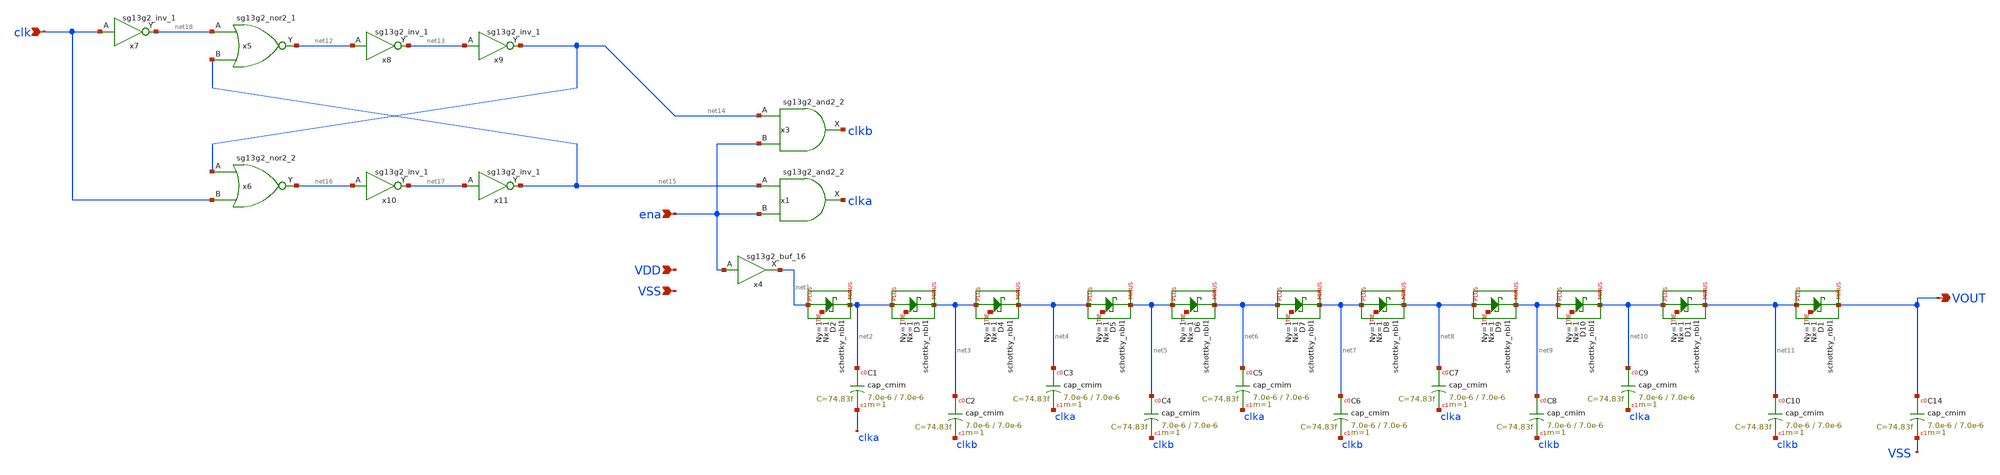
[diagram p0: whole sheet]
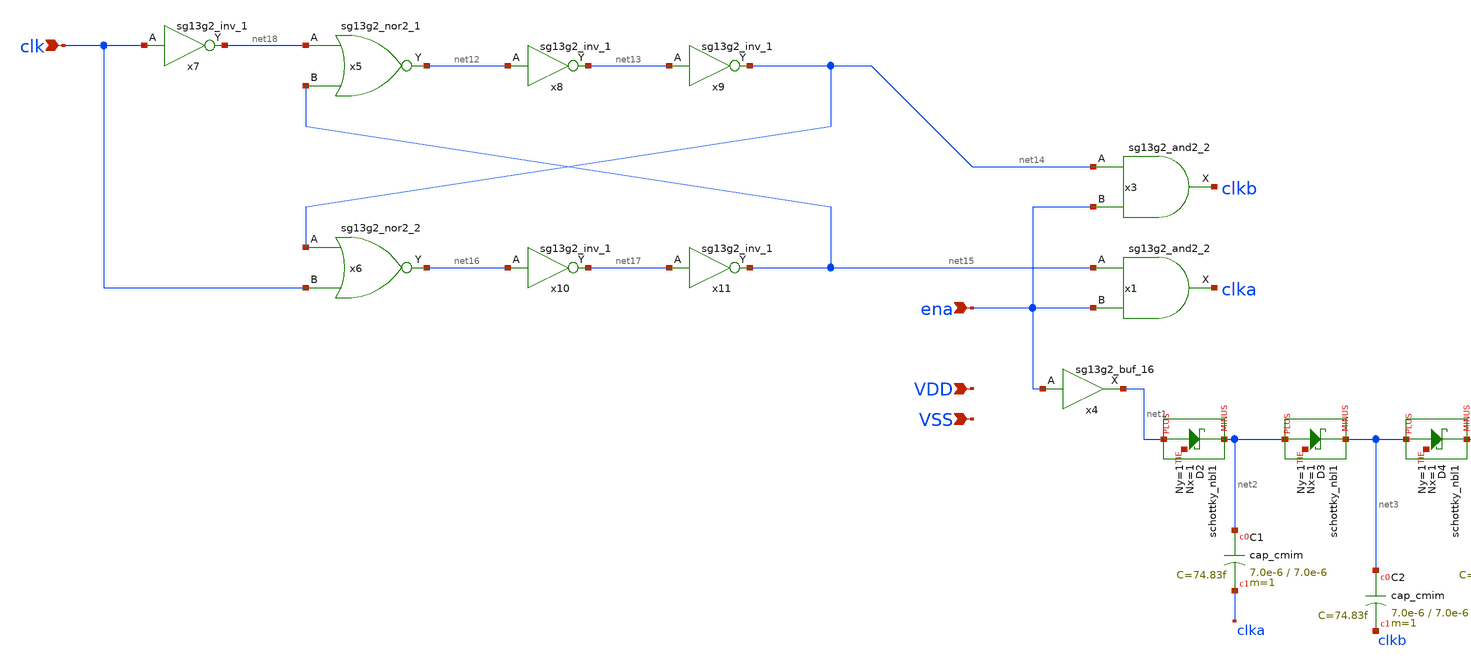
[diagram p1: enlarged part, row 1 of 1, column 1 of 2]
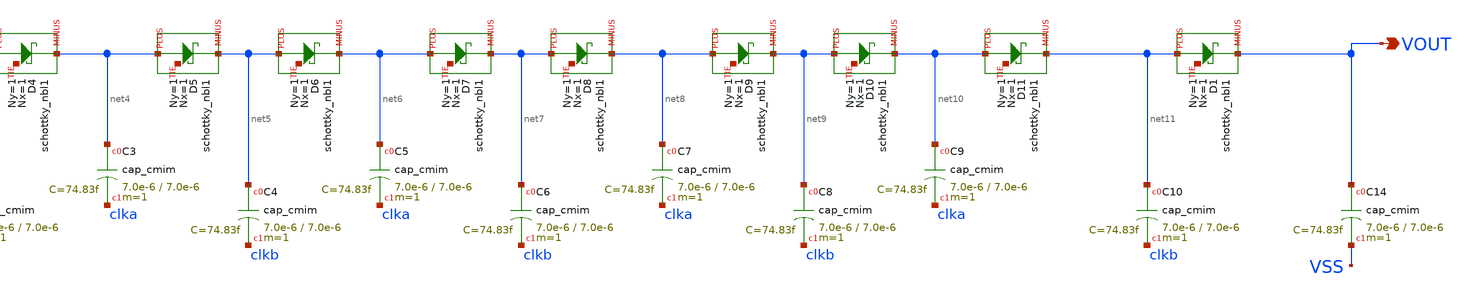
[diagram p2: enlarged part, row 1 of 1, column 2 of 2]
** sch_path: ihp130_cells/Schottky_PosChargePump/schottky_pump.sch
* IHP-GmbH/IHP-Open-PDK/ihp-sg13g2/libs.tech/xschem/sg13g2_stdcells/sg13g2_nor2_1.sch:
* Copyright 2023 IHP PDK Authors
* Licensed under the Apache License, Version 2.0 (the "License");
**.subckt schottky_pump clk ena VDD VSS VOUT
*.ipin clk
*.ipin ena
*.ipin VDD
*.ipin VSS
*.opin VOUT
XC1 net2 clka cap_cmim w=7.0e-6 l=7.0e-6 m=1 mm_ok=1
x1 clka net15 ena VDD VSS sg13g2_and2_2
x3 clkb net14 ena VDD VSS sg13g2_and2_2
x4 net1 ena VDD VSS sg13g2_buf_16
XD2 net1 net2 net19 schottky_nbl1 Nx=1 Ny=1
XD3 net2 net3 net20 schottky_nbl1 Nx=1 Ny=1
XD4 net3 net4 net21 schottky_nbl1 Nx=1 Ny=1
XD5 net4 net5 net22 schottky_nbl1 Nx=1 Ny=1
XD6 net5 net6 net23 schottky_nbl1 Nx=1 Ny=1
XD7 net6 net7 net24 schottky_nbl1 Nx=1 Ny=1
XD8 net7 net8 net25 schottky_nbl1 Nx=1 Ny=1
XD9 net8 net9 net26 schottky_nbl1 Nx=1 Ny=1
XD10 net9 net10 net27 schottky_nbl1 Nx=1 Ny=1
XD11 net10 net11 net28 schottky_nbl1 Nx=1 Ny=1
XC2 net3 clkb cap_cmim w=7.0e-6 l=7.0e-6 m=1 mm_ok=1
XC3 net4 clka cap_cmim w=7.0e-6 l=7.0e-6 m=1 mm_ok=1
XC4 net5 clkb cap_cmim w=7.0e-6 l=7.0e-6 m=1 mm_ok=1
XC5 net6 clka cap_cmim w=7.0e-6 l=7.0e-6 m=1 mm_ok=1
XC6 net7 clkb cap_cmim w=7.0e-6 l=7.0e-6 m=1 mm_ok=1
XC7 net8 clka cap_cmim w=7.0e-6 l=7.0e-6 m=1 mm_ok=1
XC8 net9 clkb cap_cmim w=7.0e-6 l=7.0e-6 m=1 mm_ok=1
XC9 net10 clka cap_cmim w=7.0e-6 l=7.0e-6 m=1 mm_ok=1
XC14 VOUT VSS cap_cmim w=7.0e-6 l=7.0e-6 m=1 mm_ok=1
XD1 net11 VOUT net29 schottky_nbl1 Nx=1 Ny=1
XC10 net11 clkb cap_cmim w=7.0e-6 l=7.0e-6 m=1 mm_ok=1
x5 net12 net18 net15 VDD VSS sg13g2_nor2_1
x6 net16 net14 clk VDD VSS sg13g2_nor2_2
x7 net18 clk VDD VSS sg13g2_inv_1
x8 net13 net12 VDD VSS sg13g2_inv_1
x9 net14 net13 VDD VSS sg13g2_inv_1
x10 net17 net16 VDD VSS sg13g2_inv_1
x11 net15 net17 VDD VSS sg13g2_inv_1
**.ends

* expanding   symbol:  sg13g2_stdcells/sg13g2_and2_2.sym # of pins=3
** sym_path: sg13g2_stdcells/sg13g2_and2_2.sym
** sch_path: sg13g2_stdcells/sg13g2_and2_2.sch
.subckt sg13g2_and2_2 X A B VDD VSS
*.ipin A
*.ipin B
*.opin X
*.iopin VDD
*.iopin VSS
XM1 net1 A net2 VSS sg13_lv_nmos w=640.00n l=130.00n ng=1 m=1 mm_ok=1
XM2 net2 B VSS VSS sg13_lv_nmos w=640.00n l=130.00n ng=1 m=1 mm_ok=1
XM3 X net1 VSS VSS sg13_lv_nmos w=1.48u l=130.00n ng=2 m=1 mm_ok=1
XM4 net1 B VDD VDD sg13_lv_pmos w=840.00n l=130.00n ng=1 m=1 mm_ok=1
XM5 net1 A VDD VDD sg13_lv_pmos w=840.00n l=130.00n ng=1 m=1 mm_ok=1
XM6 X net1 VDD VDD sg13_lv_pmos w=2.24u l=130.00n ng=2 m=1 mm_ok=1
.ends


* expanding   symbol:  sg13g2_stdcells/sg13g2_buf_16.sym # of pins=2
** sym_path: sg13g2_stdcells/sg13g2_buf_16.sym
** sch_path: sg13g2_stdcells/sg13g2_buf_16.sch
.subckt sg13g2_buf_16 X A VDD VSS
*.ipin A
*.opin X
*.iopin VDD
*.iopin VSS
XM1 net1 A VSS VSS sg13_lv_nmos w=4.44u l=130.00n ng=6 m=1 mm_ok=1
XM2 X net1 VSS VSS sg13_lv_nmos w=11.84u l=130.00n ng=16 m=1 mm_ok=1
XM3 net1 A VDD VDD sg13_lv_pmos w=6.72u l=130.00n ng=6 m=1 mm_ok=1
XM4 X net1 VDD VDD sg13_lv_pmos w=17.92u l=130.00n ng=16 m=1 mm_ok=1
.ends


* expanding   symbol:
*+  /srv/cadsp/pdks/open_pdks/IHP-Open-PDK/ihp-sg13g2/libs.tech/xschem/sg13g2_stdcells/sg13g2_nor2_1.sym # of pins=3
** sym_path: /srv/cadsp/pdks/open_pdks/IHP-Open-PDK/ihp-sg13g2/libs.tech/xschem/sg13g2_stdcells/sg13g2_nor2_1.sym
** sch_path: /srv/cadsp/pdks/open_pdks/IHP-Open-PDK/ihp-sg13g2/libs.tech/xschem/sg13g2_stdcells/sg13g2_nor2_1.sch
.subckt sg13g2_nor2_1 Y A B VDD VSS
*.opin Y
*.ipin B
*.ipin A
*.iopin VDD
*.iopin VSS
XM1 Y A VSS VSS sg13_lv_nmos w=740.00n l=130.00n ng=1 m=1 mm_ok=1
XM2 Y B VSS VSS sg13_lv_nmos w=740.00n l=130.00n ng=1 m=1 mm_ok=1
XM3 net1 A VDD VDD sg13_lv_pmos w=1.12u l=130.00n ng=1 m=1 mm_ok=1
XM4 Y B net1 VDD sg13_lv_pmos w=1.12u l=130.00n ng=1 m=1 mm_ok=1
.ends


* expanding   symbol:
*+  /srv/cadsp/pdks/open_pdks/IHP-Open-PDK/ihp-sg13g2/libs.tech/xschem/sg13g2_stdcells/sg13g2_nor2_2.sym # of pins=3
** sym_path: /srv/cadsp/pdks/open_pdks/IHP-Open-PDK/ihp-sg13g2/libs.tech/xschem/sg13g2_stdcells/sg13g2_nor2_2.sym
** sch_path: /srv/cadsp/pdks/open_pdks/IHP-Open-PDK/ihp-sg13g2/libs.tech/xschem/sg13g2_stdcells/sg13g2_nor2_2.sch
.subckt sg13g2_nor2_2 Y A B VDD VSS
*.opin Y
*.ipin B
*.ipin A
*.iopin VDD
*.iopin VSS
XM1 Y A VSS VSS sg13_lv_nmos w=1.48u l=130.00n ng=2 m=1 mm_ok=1
XM2 Y B VSS VSS sg13_lv_nmos w=1.48u l=130.00n ng=2 m=1 mm_ok=1
XM3 net1 A VDD VDD sg13_lv_pmos w=2.24u l=130.00n ng=2 m=1 mm_ok=1
XM4 Y B net1 VDD sg13_lv_pmos w=2.24u l=130.00n ng=2 m=1 mm_ok=1
.ends


* expanding   symbol:  sg13g2_stdcells/sg13g2_inv_1.sym # of pins=2
** sym_path: sg13g2_stdcells/sg13g2_inv_1.sym
** sch_path: sg13g2_stdcells/sg13g2_inv_1.sch
.subckt sg13g2_inv_1 Y A VDD VSS
*.opin Y
*.ipin A
*.iopin VDD
*.iopin VSS
XM1 Y A VSS VSS sg13_lv_nmos w=740.00n l=130.00n ng=1 m=1 mm_ok=1
XM2 Y A VDD VDD sg13_lv_pmos w=1.12u l=130.00n ng=1 m=1 mm_ok=1
.ends

.end
